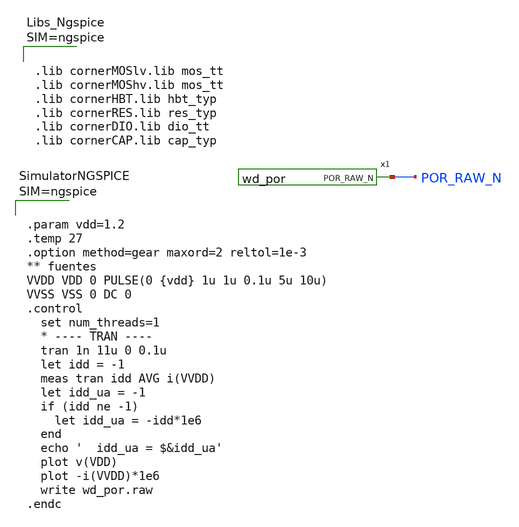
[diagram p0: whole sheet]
** sch_path: design/blocks/por/schematic/wd_por_tb.sch
**.subckt wd_por_tb
x1 POR_RAW_N VDD VSS wd_por
**** begin user architecture code



.lib cornerMOSlv.lib mos_tt
.lib cornerMOShv.lib mos_tt
.lib cornerHBT.lib hbt_typ
.lib cornerRES.lib res_typ
.lib cornerDIO.lib dio_tt
.lib cornerCAP.lib cap_typ






.param vdd=1.2
.temp 27
.option method=gear maxord=2 reltol=1e-3
** fuentes
VVDD VDD 0 PULSE(0 {vdd} 1u 1u 0.1u 5u 10u)
VVSS VSS 0 DC 0
.control
  set num_threads=1
  * ---- TRAN ----
  tran 1n 11u 0 0.1u
  let idd = -1
  meas tran idd AVG i(VVDD)
  let idd_ua = -1
  if (idd ne -1)
    let idd_ua = -idd*1e6
  end
  echo '  idd_ua = $&idd_ua'
  plot v(VDD)
  plot -i(VVDD)*1e6
  write wd_por.raw
.endc



**** end user architecture code
**.ends

* expanding   symbol:  wd_por.sym # of pins=1
** sym_path: design/blocks/por/schematic/wd_por.sym
** sch_path: design/blocks/por/schematic/wd_por.sch
.subckt wd_por POR_RAW_N VDD VSS
*.opin POR_RAW_N
XR1 VDD net1 VSS rhigh w=0.5e-6 l=360e-6 m=1 b=0 mm_ok=1
XR2 net1 VSS VSS rhigh w=0.5e-6 l=385e-6 m=1 b=0 mm_ok=1
XM1 net2 net1 VSS VSS sg13_lv_nmos w=0.3u l=9.9u ng=1 m=1 mm_ok=1
x1 net4 net2 VDD VSS sg13g2_inv_1
XR3 VDD net3 VSS rhigh w=0.5e-6 l=65e-6 m=1 b=0 mm_ok=1
XC1 net3 VSS cap_cmim w=64.0e-6 l=64.0e-6 m=1 mm_ok=1
XM3 net3 VDD VDD VDD sg13_lv_pmos w=2u l=0.13u ng=1 m=1 mm_ok=1
x2 POR_RAW_N net3 net4 VDD VSS sg13g2_and2_1
XR4 VDD net2 VSS rhigh w=0.5e-6 l=675e-6 m=1 b=0 mm_ok=1
.ends


* expanding   symbol:  sg13g2_inv_1.sym # of pins=2
** sym_path: sg13g2_inv_1.sym
** sch_path: sg13g2_inv_1.sch
.subckt sg13g2_inv_1 Y A VDD VSS
*.opin Y
*.ipin A
*.iopin VDD
*.iopin VSS
XM1 Y A VSS VSS sg13_lv_nmos w=740.00n l=130.00n ng=1 m=1 mm_ok=1
XM2 Y A VDD VDD sg13_lv_pmos w=1.12u l=130.00n ng=1 m=1 mm_ok=1
.ends


* expanding   symbol:  sg13g2_and2_1.sym # of pins=3
** sym_path: sg13g2_and2_1.sym
** sch_path: sg13g2_and2_1.sch
.subckt sg13g2_and2_1 X A B VDD VSS
*.ipin A
*.ipin B
*.opin X
*.iopin VDD
*.iopin VSS
XM1 net1 A net2 VSS sg13_lv_nmos w=640.00n l=130.00n ng=1 m=1 mm_ok=1
XM2 net2 B VSS VSS sg13_lv_nmos w=640.00n l=130.00n ng=1 m=1 mm_ok=1
XM3 X net1 VSS VSS sg13_lv_nmos w=740.00n l=130.00n ng=1 m=1 mm_ok=1
XM4 net1 B VDD VDD sg13_lv_pmos w=840.00n l=130.00n ng=1 m=1 mm_ok=1
XM5 net1 A VDD VDD sg13_lv_pmos w=840.00n l=130.00n ng=1 m=1 mm_ok=1
XM6 X net1 VDD VDD sg13_lv_pmos w=1.12u l=130.00n ng=1 m=1 mm_ok=1
.ends

.end
